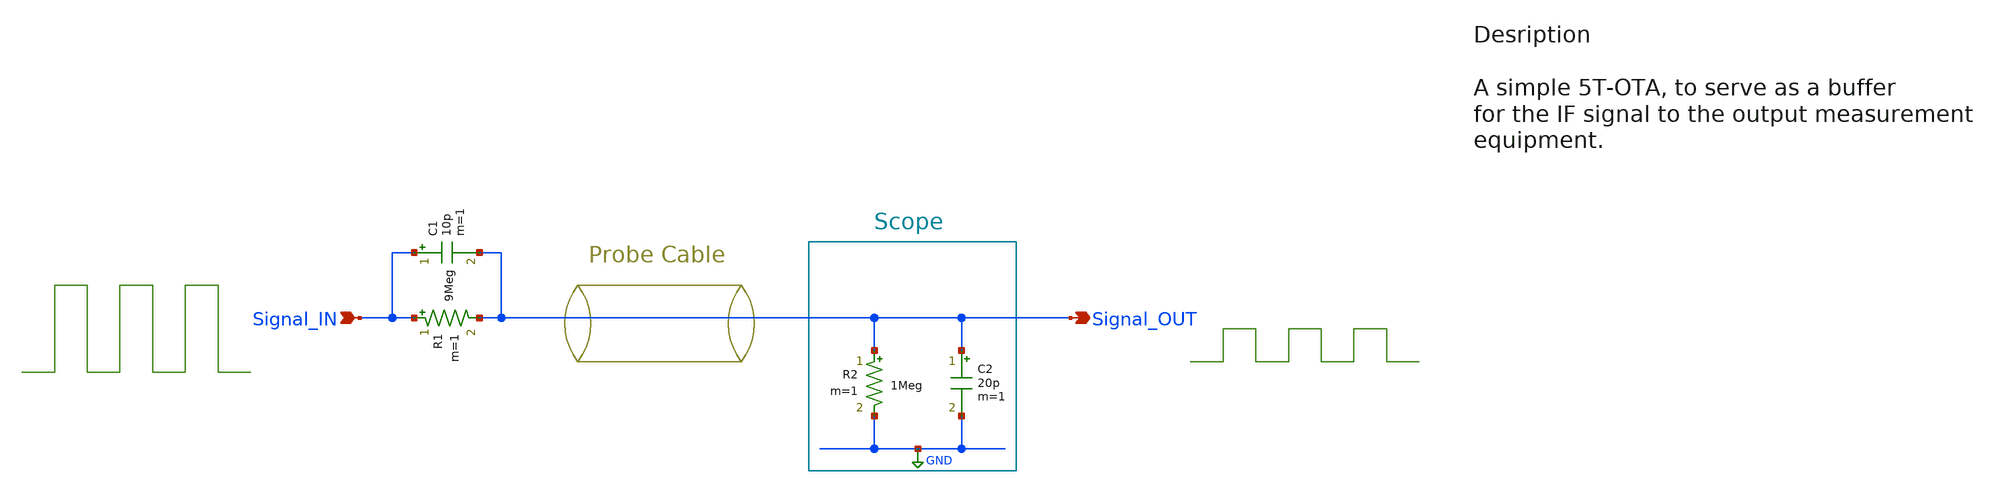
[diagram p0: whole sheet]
** sch_path: src/design_xsch/Oscilloscope-probe.sch
**.subckt Oscilloscope-probe Signal_IN Signal_OUT
*.ipin Signal_IN
*.opin Signal_OUT
R1 Signal_IN Signal_OUT 9Meg m=1
C1 Signal_IN Signal_OUT 10p m=1
R2 Signal_OUT GND 1Meg m=1
C2 Signal_OUT GND 20p m=1
**** begin user architecture code

.include $::180MCU_MODELS/design.ngspice
.lib $::180MCU_MODELS/sm141064.ngspice typical
.lib $::180MCU_MODELS/sm141064.ngspice mimcap_typical
.lib $::180MCU_MODELS/sm141064.ngspice cap_mim
.lib $::180MCU_MODELS/sm141064.ngspice res_typical


**** end user architecture code
**.ends
.GLOBAL GND
.end
